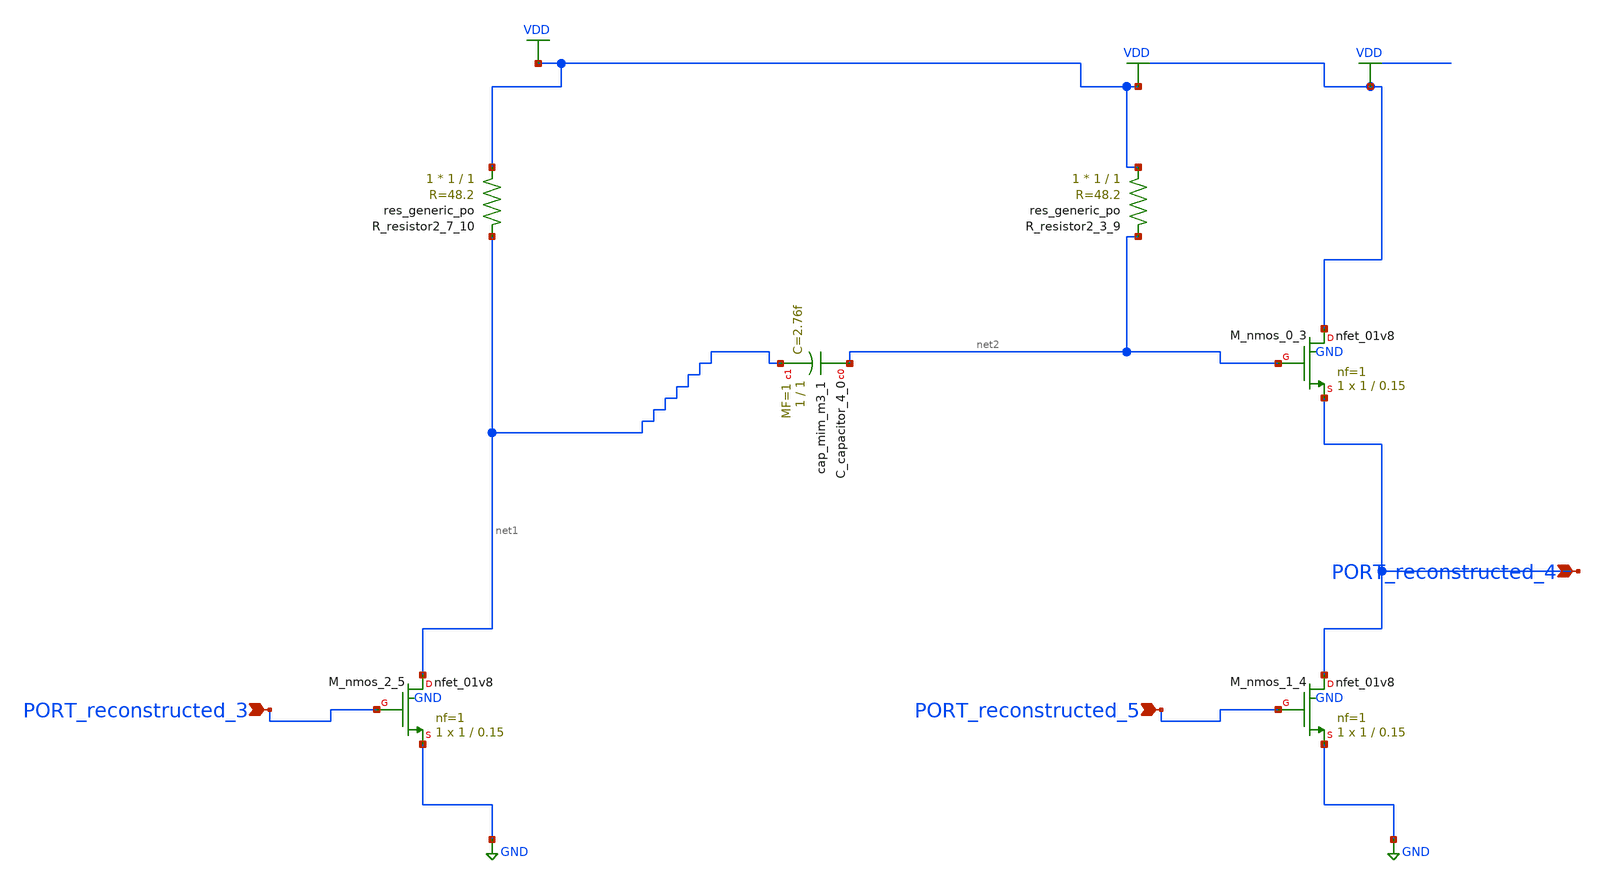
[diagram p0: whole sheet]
** sch_path: schematics/AMSNet/318.sch
**.subckt 318 PORT_reconstructed_4 PORT_reconstructed_5 PORT_reconstructed_3
*.ipin PORT_reconstructed_4
*.ipin PORT_reconstructed_5
*.ipin PORT_reconstructed_3
XC_capacitor_4_0 net2 net1 sky130_fd_pr__cap_mim_m3_1 W=1 L=1 MF=1 m=1
XM_nmos_0_3 VDD net2 PORT_reconstructed_4 GND sky130_fd_pr__nfet_01v8 L=0.15 W=1 nf=1 ad='int((1 + 1)/2) * 1 / 1 * 0.29'
+ as='int((1 + 2)/2) * 1 / 1 * 0.29' pd='2*int((1 + 1)/2) * (1 / 1 + 0.29)' ps='2*int((1 + 2)/2) * (1 / 1 + 0.29)'
+ nrd='0.29 / 1 ' nrs='0.29 / 1 ' sa=0 sb=0 sd=0 mult=1 m=1
XM_nmos_1_4 PORT_reconstructed_4 PORT_reconstructed_5 GND GND sky130_fd_pr__nfet_01v8 L=0.15 W=1 nf=1
+ ad='int((1 + 1)/2) * 1 / 1 * 0.29' as='int((1 + 2)/2) * 1 / 1 * 0.29' pd='2*int((1 + 1)/2) * (1 / 1 + 0.29)'
+ ps='2*int((1 + 2)/2) * (1 / 1 + 0.29)' nrd='0.29 / 1 ' nrs='0.29 / 1 ' sa=0 sb=0 sd=0 mult=1 m=1
XM_nmos_2_5 net1 PORT_reconstructed_3 GND GND sky130_fd_pr__nfet_01v8 L=0.15 W=1 nf=1 ad='int((1 + 1)/2) * 1 / 1 * 0.29'
+ as='int((1 + 2)/2) * 1 / 1 * 0.29' pd='2*int((1 + 1)/2) * (1 / 1 + 0.29)' ps='2*int((1 + 2)/2) * (1 / 1 + 0.29)'
+ nrd='0.29 / 1 ' nrs='0.29 / 1 ' sa=0 sb=0 sd=0 mult=1 m=1
XR_resistor2_3_9 VDD net2 sky130_fd_pr__res_generic_po W=1 L=1 m=1
XR_resistor2_7_10 VDD net1 sky130_fd_pr__res_generic_po W=1 L=1 m=1
**.ends
.GLOBAL GND
.GLOBAL VDD
.end
